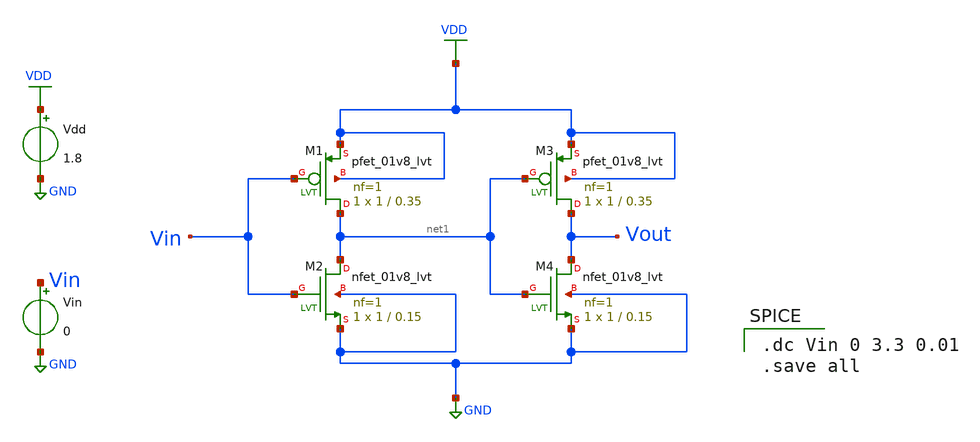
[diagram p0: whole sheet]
** sch_path: buffer/buffer.sch
**.subckt buffer
XM1 net1 Vin VDD VDD sky130_fd_pr__pfet_01v8_lvt L=0.35 W=1 nf=1 ad='int((1 + 1)/2) * 1 / 1 * 0.29' as='int((1 + 2)/2) * 1 / 1 * 0.29'
+ pd='2*int((1 + 1)/2) * (1 / 1 + 0.29)' ps='2*int((1 + 2)/2) * (1 / 1 + 0.29)' nrd='0.29 / 1 ' nrs='0.29 / 1 '
+ sa=0 sb=0 sd=0 mult=1 m=1
XM2 net1 Vin GND GND sky130_fd_pr__nfet_01v8_lvt L=0.15 W=1 nf=1 ad='int((1 + 1)/2) * 1 / 1 * 0.29' as='int((1 + 2)/2) * 1 / 1 * 0.29'
+ pd='2*int((1 + 1)/2) * (1 / 1 + 0.29)' ps='2*int((1 + 2)/2) * (1 / 1 + 0.29)' nrd='0.29 / 1 ' nrs='0.29 / 1 '
+ sa=0 sb=0 sd=0 mult=1 m=1
Vdd VDD GND 1.8
.save i(vdd)
Vin Vin GND 0
.save i(vin)
XM3 Vout net1 VDD VDD sky130_fd_pr__pfet_01v8_lvt L=0.35 W=1 nf=1 ad='int((1 + 1)/2) * 1 / 1 * 0.29'
+ as='int((1 + 2)/2) * 1 / 1 * 0.29' pd='2*int((1 + 1)/2) * (1 / 1 + 0.29)' ps='2*int((1 + 2)/2) * (1 / 1 + 0.29)'
+ nrd='0.29 / 1 ' nrs='0.29 / 1 ' sa=0 sb=0 sd=0 mult=1 m=1
XM4 Vout net1 GND GND sky130_fd_pr__nfet_01v8_lvt L=0.15 W=1 nf=1 ad='int((1 + 1)/2) * 1 / 1 * 0.29'
+ as='int((1 + 2)/2) * 1 / 1 * 0.29' pd='2*int((1 + 1)/2) * (1 / 1 + 0.29)' ps='2*int((1 + 2)/2) * (1 / 1 + 0.29)'
+ nrd='0.29 / 1 ' nrs='0.29 / 1 ' sa=0 sb=0 sd=0 mult=1 m=1
**** begin user architecture code


.lib /usr/local/share/pdk/sky130B/libs.tech/ngspice/sky130.lib.spice tt
.option wnflag=1

*--- Run ----------------------------------

.control
run
wrdata untitled.raw V(Vout) V(Vin) V(VDD) I(Vdd)
.endc



.dc Vin 0 3.3 0.01
.save all

**** end user architecture code
**.ends
.GLOBAL GND
.GLOBAL VDD
.end
